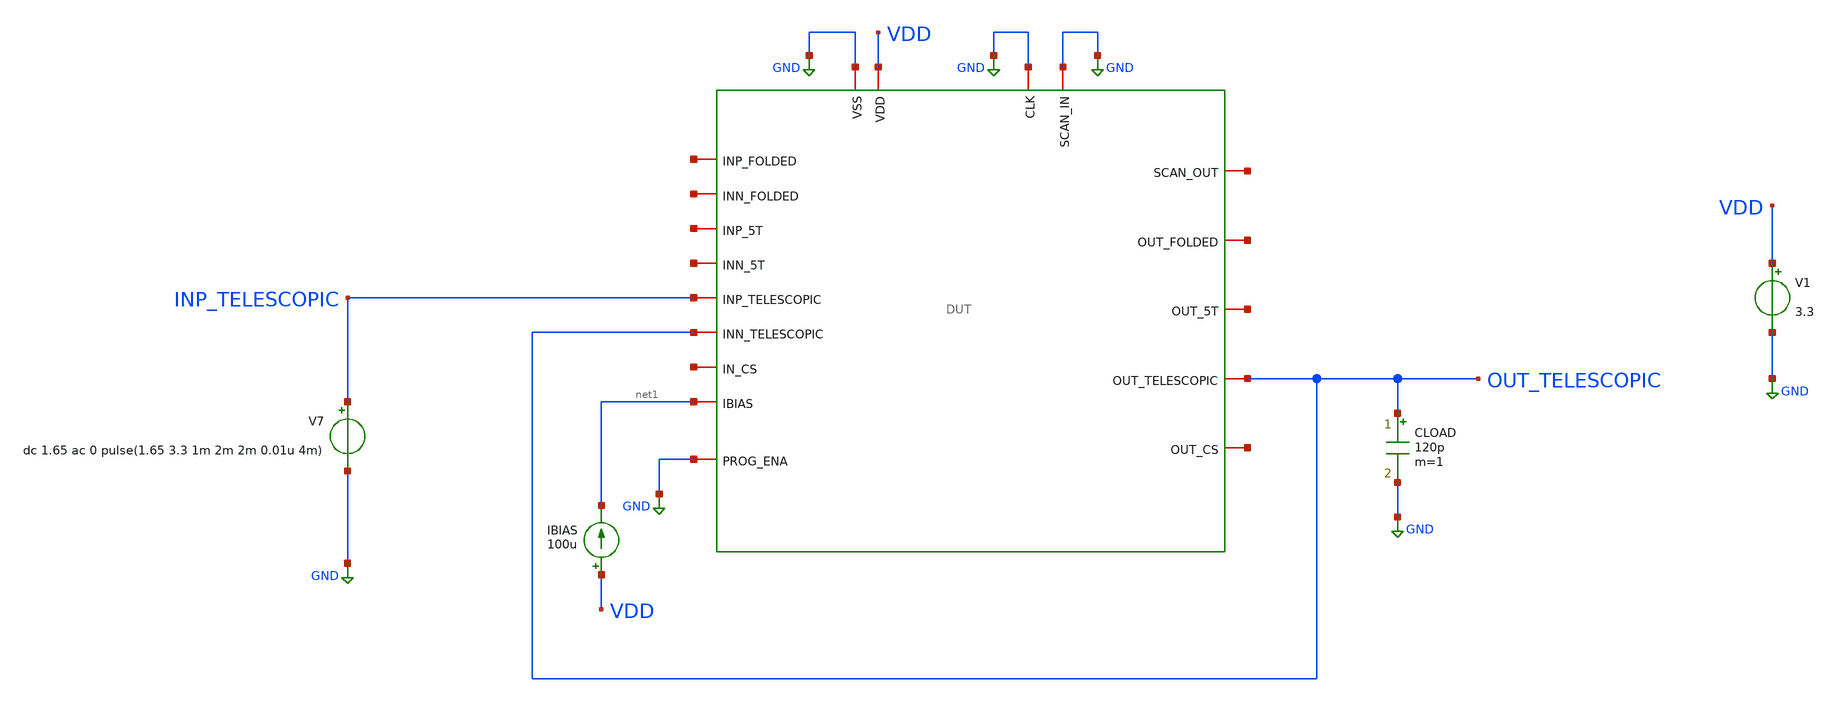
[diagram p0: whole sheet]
** sch_path: designs/libs/verification/ota_telescopic/default/large_signal_upper_swing_tb.sch
**.subckt large_signal_upper_swing_tb
x1 GND net2 GND GND VDD net3 net4 net5 net1 net6 net7 net8 INP_TELESCOPIC OUT_TELESCOPIC net9 net10
+ OUT_TELESCOPIC GND DUT
V1 VDD GND 3.3
CLOAD OUT_TELESCOPIC GND 120p m=1
V7 INP_TELESCOPIC GND dc 1.65 ac 0 pulse(1.65 3.3 1m 2m 2m 0.01u 4m)
IBIAS VDD net1 100u
**** begin user architecture code

.include $::180MCU_MODELS/design.ngspice
.lib $::180MCU_MODELS/sm141064.ngspice typical



.control
tran 1u 5m

plot v(out_telescopic) v(inp_telescopic)

let error = v(out_telescopic) - v(inp_telescopic)
plot error

meas tran t_clip when error = -0.019 cross = 1
print t_clip

meas tran vout_clip find v(out_telescopic) at = t_clip
meas tran vin_clip find v(inp_telescopic) at = t_clip
print vout_clip vin_clip
.endc


**** end user architecture code
**.ends
.GLOBAL GND
.end
